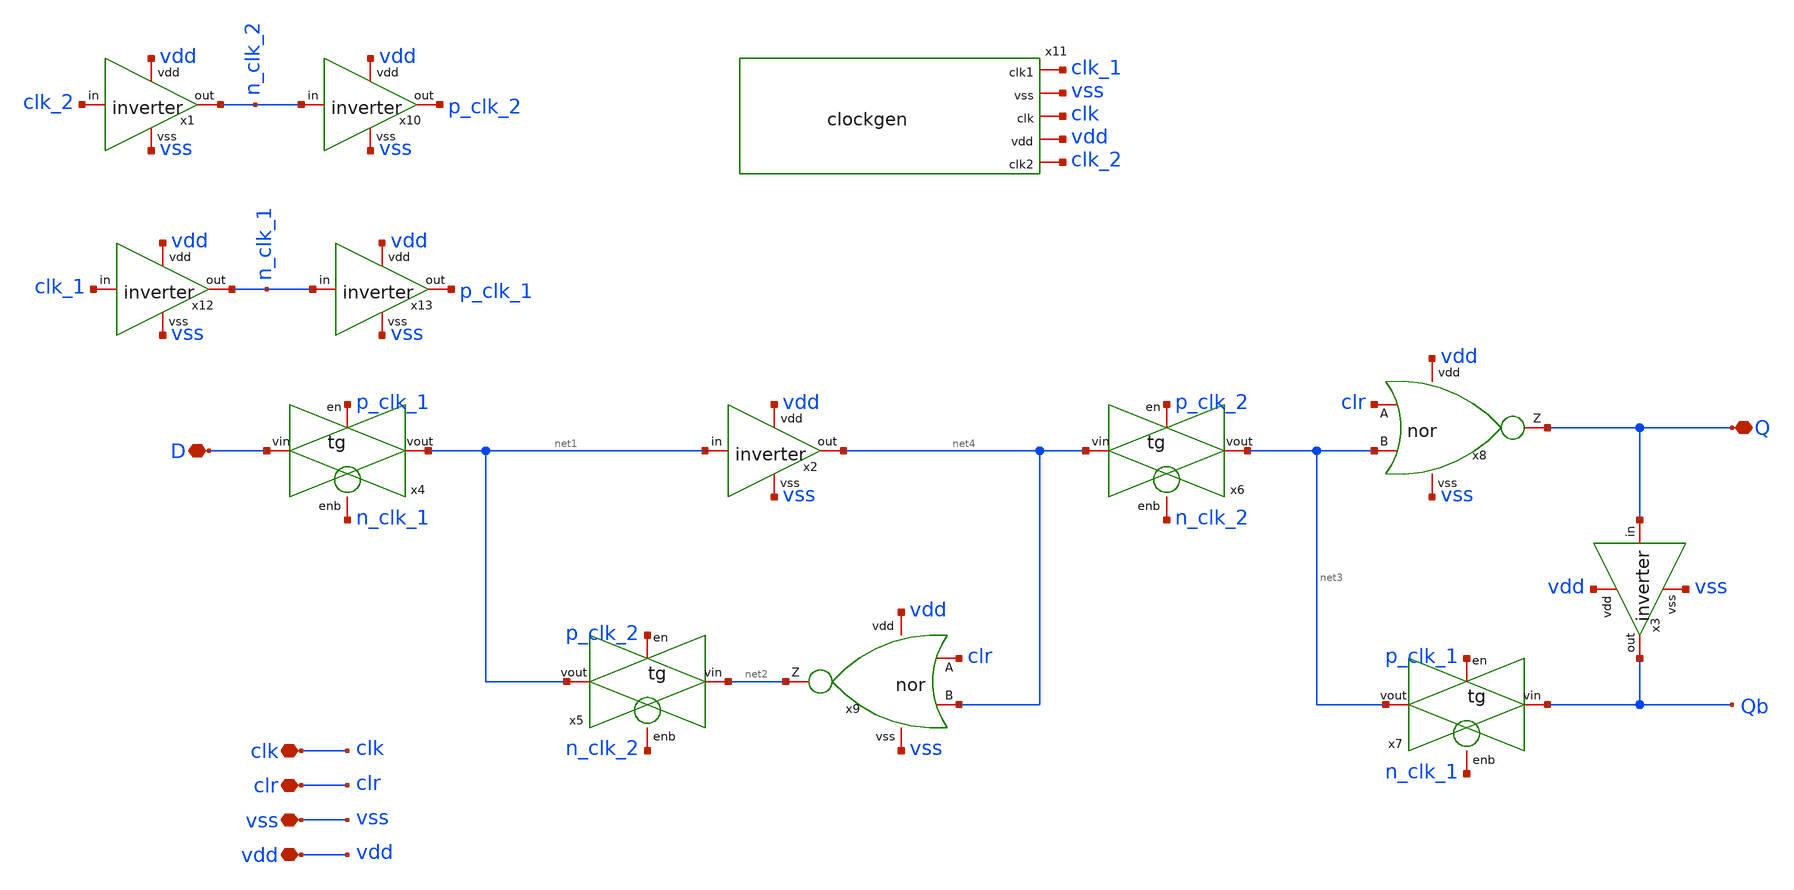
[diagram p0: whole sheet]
** sch_path: designs/sch/dffc2.sch
**.subckt dffc2 clk clr vss vdd D Q
*.iopin clk
*.iopin clr
*.iopin vss
*.iopin vdd
*.iopin D
*.iopin Q
x1 vdd n_clk_2 clk_2 vss inverter
x2 vdd net4 net1 vss inverter
x3 vdd Qb Q vss inverter
x4 D n_clk_1 p_clk_1 net1 tg
x8 vdd Q clr net3 vss nor
x9 vdd net2 clr net4 vss nor
x5 net2 n_clk_2 p_clk_2 net1 tg
x6 net4 n_clk_2 p_clk_2 net3 tg
x7 Qb n_clk_1 p_clk_1 net3 tg
x10 vdd p_clk_2 n_clk_2 vss inverter
x11 clk_1 vss clk vdd clk_2 clockgen
x12 vdd n_clk_1 clk_1 vss inverter
x13 vdd p_clk_1 n_clk_1 vss inverter
**.ends

* expanding   symbol:  /foss/designs/sch/inverter.sym # of pins=4
** sym_path: designs/inverter.sym
** sch_path: designs/inverter.sch
.subckt inverter vdd out in vss
*.iopin out
*.iopin vss
*.iopin vdd
*.iopin in
XM2 out in vss vss sky130_fd_pr__nfet_01v8 L=0.15 W=0.75 nf=1 ad='int((nf+1)/2) * W/nf * 0.29' as='int((nf+2)/2) * W/nf * 0.29'
+ pd='2*int((nf+1)/2) * (W/nf + 0.29)' ps='2*int((nf+2)/2) * (W/nf + 0.29)' nrd='0.29 / W' nrs='0.29 / W'
+ sa=0 sb=0 sd=0 mult=1 m=1
XM1 out in vdd vdd sky130_fd_pr__pfet_01v8 L=0.15 W=1.5 nf=1 ad='int((nf+1)/2) * W/nf * 0.29' as='int((nf+2)/2) * W/nf * 0.29'
+ pd='2*int((nf+1)/2) * (W/nf + 0.29)' ps='2*int((nf+2)/2) * (W/nf + 0.29)' nrd='0.29 / W' nrs='0.29 / W'
+ sa=0 sb=0 sd=0 mult=1 m=1
.ends


* expanding   symbol:  /foss/designs/sch/tg.sym # of pins=4
** sym_path: designs/tg.sym
** sch_path: designs/tg.sch
.subckt tg vin enb en vout
*.iopin vin
*.iopin vout
*.iopin enb
*.iopin en
XM1 vin en vout enb sky130_fd_pr__nfet_01v8 L=0.15 W=0.75 nf=1 ad='int((nf+1)/2) * W/nf * 0.29' as='int((nf+2)/2) * W/nf * 0.29'
+ pd='2*int((nf+1)/2) * (W/nf + 0.29)' ps='2*int((nf+2)/2) * (W/nf + 0.29)' nrd='0.29 / W' nrs='0.29 / W'
+ sa=0 sb=0 sd=0 mult=1 m=1
XM2 vout enb vin en sky130_fd_pr__pfet_01v8 L=0.15 W=1.5 nf=1 ad='int((nf+1)/2) * W/nf * 0.29' as='int((nf+2)/2) * W/nf * 0.29'
+ pd='2*int((nf+1)/2) * (W/nf + 0.29)' ps='2*int((nf+2)/2) * (W/nf + 0.29)' nrd='0.29 / W' nrs='0.29 / W'
+ sa=0 sb=0 sd=0 mult=1 m=1
.ends


* expanding   symbol:  /foss/designs/sch/nor.sym # of pins=5
** sym_path: designs/sch/nor.sym
** sch_path: designs/sch/nor.sch
.subckt nor vdd Z A B vss
*.iopin A
*.iopin B
*.iopin vdd
*.iopin Z
*.iopin vss
XM1 Z A vss vss sky130_fd_pr__nfet_01v8 L=0.15 W=0.75 nf=1 ad='int((nf+1)/2) * W/nf * 0.29' as='int((nf+2)/2) * W/nf * 0.29'
+ pd='2*int((nf+1)/2) * (W/nf + 0.29)' ps='2*int((nf+2)/2) * (W/nf + 0.29)' nrd='0.29 / W' nrs='0.29 / W'
+ sa=0 sb=0 sd=0 mult=1 m=1
XM4 net1 B vdd vdd sky130_fd_pr__pfet_01v8 L=0.15 W=3 nf=1 ad='int((nf+1)/2) * W/nf * 0.29' as='int((nf+2)/2) * W/nf * 0.29'
+ pd='2*int((nf+1)/2) * (W/nf + 0.29)' ps='2*int((nf+2)/2) * (W/nf + 0.29)' nrd='0.29 / W' nrs='0.29 / W'
+ sa=0 sb=0 sd=0 mult=1 m=1
XM2 Z B vss vss sky130_fd_pr__nfet_01v8 L=0.15 W=0.75 nf=1 ad='int((nf+1)/2) * W/nf * 0.29' as='int((nf+2)/2) * W/nf * 0.29'
+ pd='2*int((nf+1)/2) * (W/nf + 0.29)' ps='2*int((nf+2)/2) * (W/nf + 0.29)' nrd='0.29 / W' nrs='0.29 / W'
+ sa=0 sb=0 sd=0 mult=1 m=1
XM3 Z A net1 vdd sky130_fd_pr__pfet_01v8 L=0.15 W=3 nf=1 ad='int((nf+1)/2) * W/nf * 0.29' as='int((nf+2)/2) * W/nf * 0.29'
+ pd='2*int((nf+1)/2) * (W/nf + 0.29)' ps='2*int((nf+2)/2) * (W/nf + 0.29)' nrd='0.29 / W' nrs='0.29 / W'
+ sa=0 sb=0 sd=0 mult=1 m=1
.ends


* expanding   symbol:  /foss/designs/sch/clockgen.sym # of pins=5
** sym_path: designs/sch/clockgen.sym
** sch_path: designs/sch/clockgen.sch
.subckt clockgen clk1 vss clk vdd clk2
*.iopin vss
*.iopin vdd
*.iopin clk1
*.iopin clk2
*.iopin clk
x1 vdd net4 clk vss inverter
x2 vdd net2 net1 clk2 vss nor
x3 vdd net3 clk1 net4 vss nor
x4 vdd net7 clk vss inverter
x6 vdd net5 net2 vss inverter
x7 vdd net6 net3 vss inverter
x5 vdd clk1 net5 vss inverter
x8 vdd clk2 net6 vss inverter
x9 vdd net1 net7 vss inverter
.ends

.end
